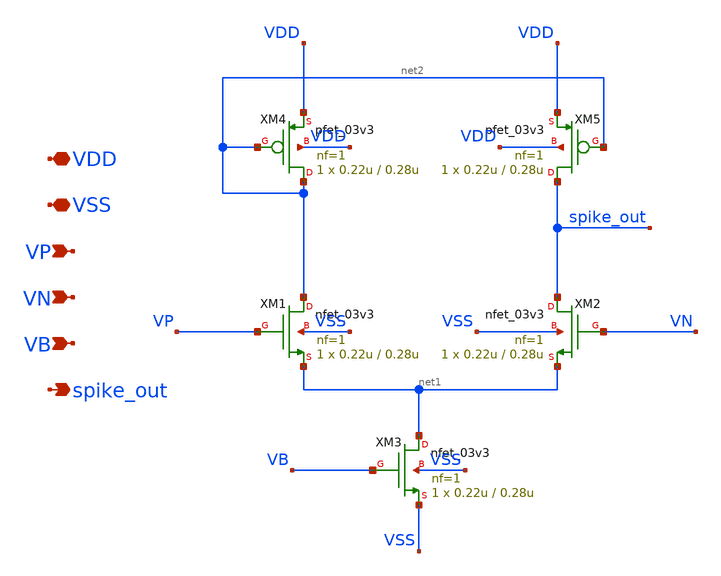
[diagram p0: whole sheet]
** sch_path: analog/neuron/spike_amplifier.sch
**.subckt spike_amplifier VDD VSS VP VN VB spike_out
*.iopin VDD
*.iopin VSS
*.ipin VP
*.ipin VN
*.ipin VB
*.opin spike_out
XM1 net2 VP net1 VSS nfet_03v3 L=0.28u W=0.22u nf=1 ad='int((nf+1)/2) * W/nf * 0.18u' as='int((nf+2)/2) * W/nf * 0.18u'
+ pd='2*int((nf+1)/2) * (W/nf + 0.18u)' ps='2*int((nf+2)/2) * (W/nf + 0.18u)' nrd='0.18u / W' nrs='0.18u / W'
+ sa=0 sb=0 sd=0 m=1
XM2 spike_out VN net1 VSS nfet_03v3 L=0.28u W=0.22u nf=1 ad='int((nf+1)/2) * W/nf * 0.18u' as='int((nf+2)/2) * W/nf * 0.18u'
+ pd='2*int((nf+1)/2) * (W/nf + 0.18u)' ps='2*int((nf+2)/2) * (W/nf + 0.18u)' nrd='0.18u / W' nrs='0.18u / W'
+ sa=0 sb=0 sd=0 m=1
XM3 net1 VB VSS VSS nfet_03v3 L=0.28u W=0.22u nf=1 ad='int((nf+1)/2) * W/nf * 0.18u' as='int((nf+2)/2) * W/nf * 0.18u'
+ pd='2*int((nf+1)/2) * (W/nf + 0.18u)' ps='2*int((nf+2)/2) * (W/nf + 0.18u)' nrd='0.18u / W' nrs='0.18u / W'
+ sa=0 sb=0 sd=0 m=1
XM4 net2 net2 VDD VDD pfet_03v3 L=0.28u W=0.22u nf=1 ad='int((nf+1)/2) * W/nf * 0.18u' as='int((nf+2)/2) * W/nf * 0.18u'
+ pd='2*int((nf+1)/2) * (W/nf + 0.18u)' ps='2*int((nf+2)/2) * (W/nf + 0.18u)' nrd='0.18u / W' nrs='0.18u / W'
+ sa=0 sb=0 sd=0 m=1
XM5 spike_out net2 VDD VDD pfet_03v3 L=0.28u W=0.22u nf=1 ad='int((nf+1)/2) * W/nf * 0.18u' as='int((nf+2)/2) * W/nf * 0.18u'
+ pd='2*int((nf+1)/2) * (W/nf + 0.18u)' ps='2*int((nf+2)/2) * (W/nf + 0.18u)' nrd='0.18u / W' nrs='0.18u / W'
+ sa=0 sb=0 sd=0 m=1
**.ends
.end
